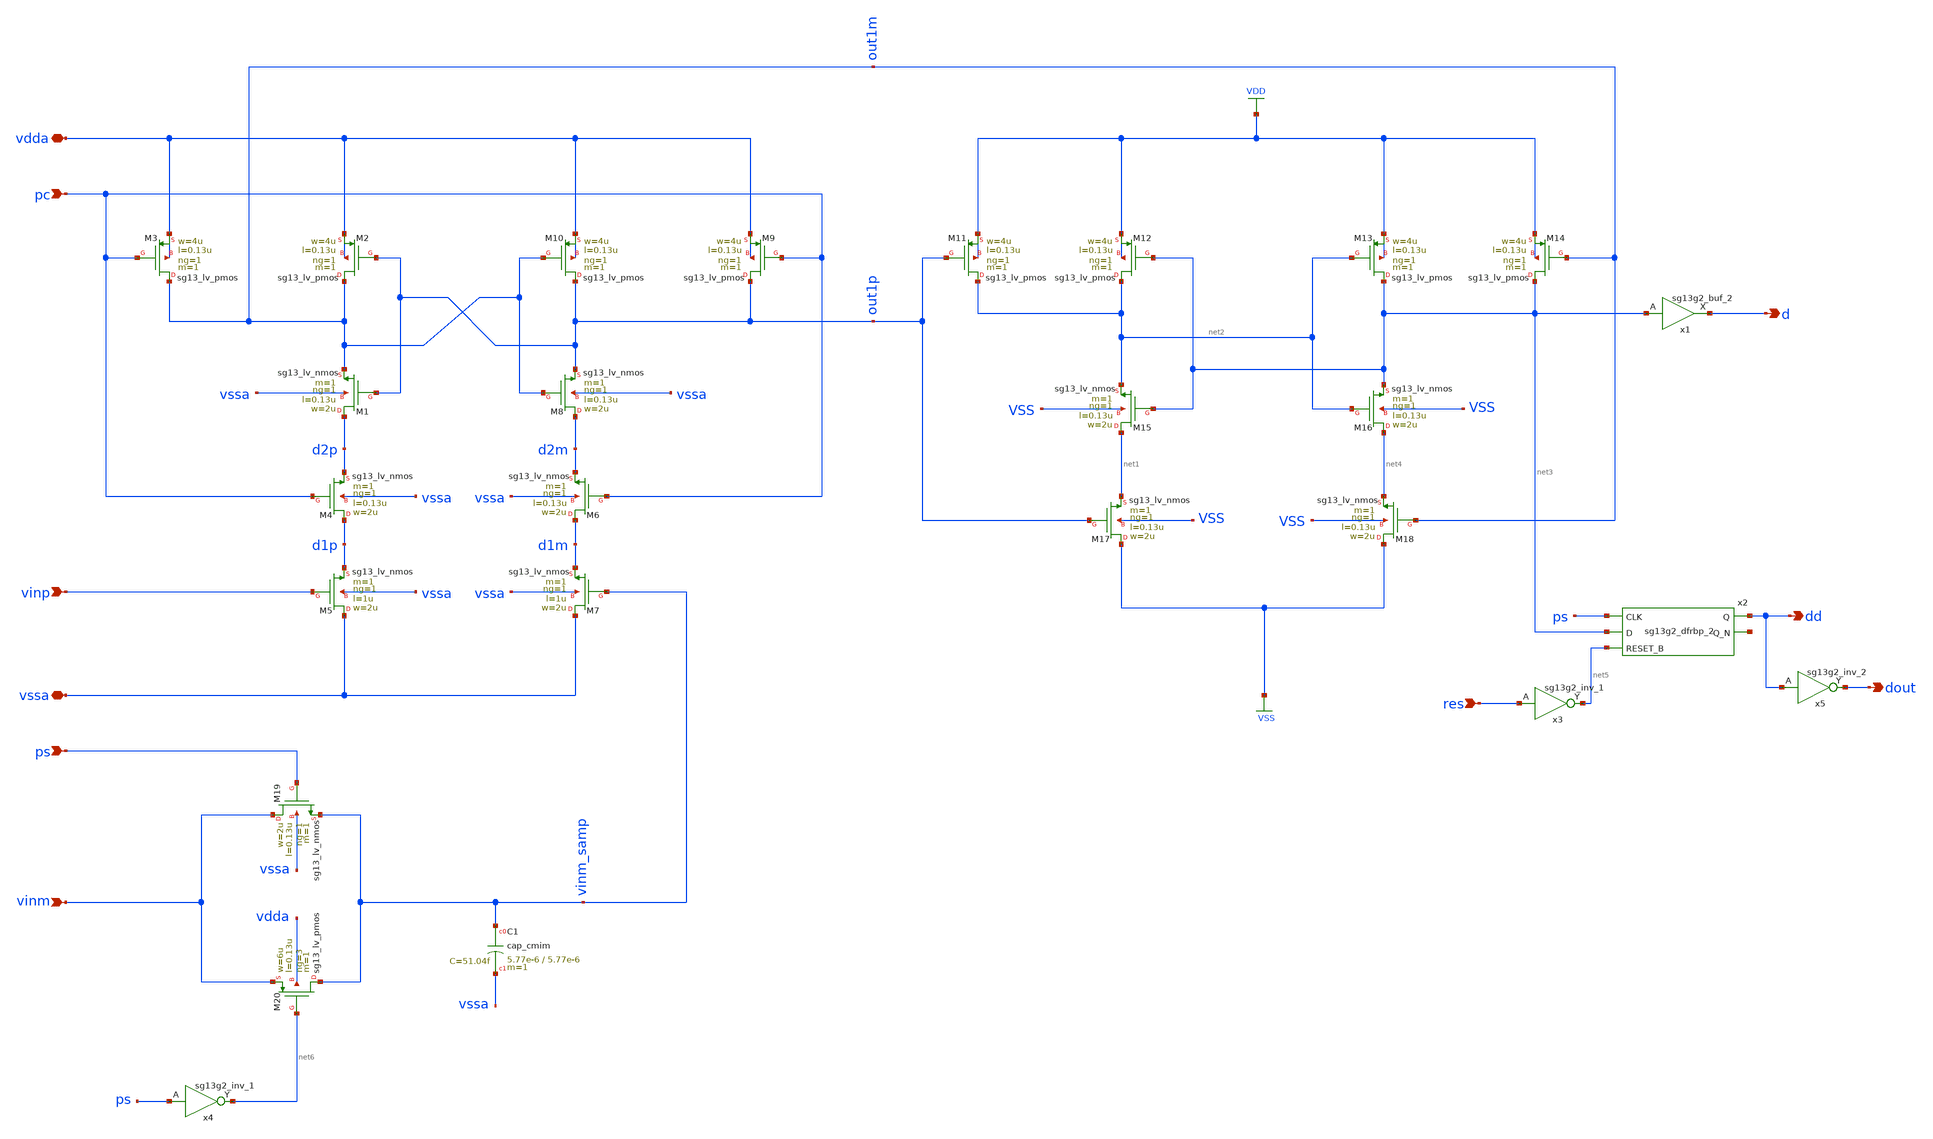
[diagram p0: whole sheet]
** sch_path: 5_Design/4_Layout/Team 3/xschem/comp_Team3.sch
* IHP-GmbH/IHP-Open-PDK/ihp-sg13g2/libs.tech/xschem/sg13g2_stdcells/sg13g2_inv_2.sch:
* Copyright 2023 IHP PDK Authors
* Licensed under the Apache License, Version 2.0 (the "License");
**.subckt comp_Team3 pc vssa vdda vinp vinm d res dd ps dout
*.ipin pc
*.iopin vssa
*.iopin vdda
*.ipin vinp
*.ipin vinm
*.opin d
*.ipin res
*.opin dd
*.ipin ps
*.opin dout
XM1 d2p out1p out1m vssa sg13_lv_nmos w=2u l=0.13u ng=1 m=1 mm_ok=1
XM2 out1m out1p vdda vdda sg13_lv_pmos w=4u l=0.13u ng=1 m=1 mm_ok=1
XM3 out1m pc vdda vdda sg13_lv_pmos w=4u l=0.13u ng=1 m=1 mm_ok=1
XM4 d1p pc d2p vssa sg13_lv_nmos w=2u l=0.13u ng=1 m=1 mm_ok=1
XM5 vssa vinp d1p vssa sg13_lv_nmos w=2u l=1u ng=1 m=1 mm_ok=1
XM6 d1m pc d2m vssa sg13_lv_nmos w=2u l=0.13u ng=1 m=1 mm_ok=1
XM7 vssa vinm_samp d1m vssa sg13_lv_nmos w=2u l=1u ng=1 m=1 mm_ok=1
XM8 d2m out1m out1p vssa sg13_lv_nmos w=2u l=0.13u ng=1 m=1 mm_ok=1
XM9 out1p pc vdda vdda sg13_lv_pmos w=4u l=0.13u ng=1 m=1 mm_ok=1
XM10 out1p out1m vdda vdda sg13_lv_pmos w=4u l=0.13u ng=1 m=1 mm_ok=1
XM11 net2 out1p VDD VDD sg13_lv_pmos w=4u l=0.13u ng=1 m=1 mm_ok=1
XM12 net2 net3 VDD VDD sg13_lv_pmos w=4u l=0.13u ng=1 m=1 mm_ok=1
XM13 net3 net2 VDD VDD sg13_lv_pmos w=4u l=0.13u ng=1 m=1 mm_ok=1
XM14 net3 out1m VDD VDD sg13_lv_pmos w=4u l=0.13u ng=1 m=1 mm_ok=1
XM15 net1 net3 net2 VSS sg13_lv_nmos w=2u l=0.13u ng=1 m=1 mm_ok=1
XM16 net4 net2 net3 VSS sg13_lv_nmos w=2u l=0.13u ng=1 m=1 mm_ok=1
XM17 VSS out1p net1 VSS sg13_lv_nmos w=2u l=0.13u ng=1 m=1 mm_ok=1
XM18 VSS out1m net4 VSS sg13_lv_nmos w=2u l=0.13u ng=1 m=1 mm_ok=1
x1 d net3 VDD VSS sg13g2_buf_2
x2 dd net7 ps net3 net5 VDD VSS sg13g2_dfrbp_2
x3 net5 res VDD VSS sg13g2_inv_1
XM19 vinm ps vinm_samp vssa sg13_lv_nmos w=2u l=0.13u ng=1 m=1 mm_ok=1
XM20 vinm_samp net6 vinm vdda sg13_lv_pmos w=6u l=0.13u ng=3 m=1 mm_ok=1
x4 net6 ps VDD VSS sg13g2_inv_1
x5 dout dd VDD VSS sg13g2_inv_2
XC1 vinm_samp vssa cap_cmim w=5.77e-6 l=5.77e-6 m=1 mm_ok=1
**.ends

* expanding   symbol:  sg13g2_stdcells/sg13g2_buf_2.sym # of pins=2
** sym_path: sg13g2_stdcells/sg13g2_buf_2.sym
** sch_path: sg13g2_stdcells/sg13g2_buf_2.sch
.subckt sg13g2_buf_2 X A VDD VSS
*.ipin A
*.opin X
*.iopin VDD
*.iopin VSS
XM1 net1 A VSS VSS sg13_lv_nmos w=640.00n l=130.00n ng=1 m=1 mm_ok=1
XM2 X net1 VSS VSS sg13_lv_nmos w=1.48u l=130.00n ng=2 m=1 mm_ok=1
XM3 net1 A VDD VDD sg13_lv_pmos w=1.000u l=130.00n ng=1 m=1 mm_ok=1
XM4 X net1 VDD VDD sg13_lv_pmos w=2.24u l=130.00n ng=2 m=1 mm_ok=1
.ends


* expanding   symbol:  sg13g2_stdcells/sg13g2_dfrbp_2.sym # of pins=5
** sym_path: sg13g2_stdcells/sg13g2_dfrbp_2.sym
** sch_path: sg13g2_stdcells/sg13g2_dfrbp_2.sch
.subckt sg13g2_dfrbp_2 Q Q_N CLK D RESET_B VDD VSS
*.ipin D
*.ipin RESET_B
*.ipin CLK
*.opin Q
*.opin Q_N
*.iopin VDD
*.iopin VSS
XM1 Db D net12 VSS sg13_lv_nmos w=420.00n l=130.00n ng=1 m=1 mm_ok=1
XM2 net12 RESET_B VSS VSS sg13_lv_nmos w=420.00n l=130.00n ng=1 m=1 mm_ok=1
XM3 net2 clkneg net11 VSS sg13_lv_nmos w=420.00n l=130.00n ng=1 m=1 mm_ok=1
XM4 net11 net3 VSS VSS sg13_lv_nmos w=420.00n l=130.00n ng=1 m=1 mm_ok=1
XM5 net3 net2 net7 VSS sg13_lv_nmos w=420.00n l=130.00n ng=1 m=1 mm_ok=1
XM6 net7 RESET_B VSS VSS sg13_lv_nmos w=420.00n l=130.00n ng=1 m=1 mm_ok=1
XM7 Q_N net2 VSS VSS sg13_lv_nmos w=1.48u l=130.00n ng=2 m=1 mm_ok=1
XM8 net1 net2 VSS VSS sg13_lv_nmos w=640.00n l=130.00n ng=1 m=1 mm_ok=1
XM9 Q net1 VSS VSS sg13_lv_nmos w=1.48u l=130.00n ng=2 m=1 mm_ok=1
XM10 clkneg CLK VSS VSS sg13_lv_nmos w=740.00n l=130.00n ng=1 m=1 mm_ok=1
XM11 clkpos clkneg VSS VSS sg13_lv_nmos w=740.00n l=130.00n ng=1 m=1 mm_ok=1
XM12 Db clkneg net4 VSS sg13_lv_nmos w=420.00n l=130.00n ng=1 m=1 mm_ok=1
XM13 net4 clkpos net10 VSS sg13_lv_nmos w=420.00n l=130.00n ng=1 m=1 mm_ok=1
XM14 net10 net5 net6 VSS sg13_lv_nmos w=420.00n l=130.00n ng=1 m=1 mm_ok=1
XM15 net6 RESET_B VSS VSS sg13_lv_nmos w=420.00n l=130.00n ng=1 m=1 mm_ok=1
XM16 net5 net4 VSS VSS sg13_lv_nmos w=740.00n l=130.00n ng=1 m=1 mm_ok=1
XM17 net5 clkpos net2 VSS sg13_lv_nmos w=740.00n l=130.00n ng=1 m=1 mm_ok=1
XM18 Db RESET_B VDD VDD sg13_lv_pmos w=420.00n l=130.00n ng=1 m=1 mm_ok=1
XM19 Db D VDD VDD sg13_lv_pmos w=420.00n l=130.00n ng=1 m=1 mm_ok=1
XM20 net9 net3 VDD VDD sg13_lv_pmos w=420.00n l=130.00n ng=1 m=1 mm_ok=1
XM21 net2 clkpos net9 VDD sg13_lv_pmos w=420.00n l=130.00n ng=1 m=1 mm_ok=1
XM22 net3 net2 VDD VDD sg13_lv_pmos w=420.00n l=130.00n ng=1 m=1 mm_ok=1
XM23 net3 RESET_B VDD VDD sg13_lv_pmos w=420.00n l=130.00n ng=1 m=1 mm_ok=1
XM24 Q_N net2 VDD VDD sg13_lv_pmos w=2.24u l=130.00n ng=2 m=1 mm_ok=1
XM25 net1 net2 VDD VDD sg13_lv_pmos w=1.000u l=130.00n ng=1 m=1 mm_ok=1
XM26 Q net1 VDD VDD sg13_lv_pmos w=2.24u l=130.00n ng=2 m=1 mm_ok=1
XM27 clkneg CLK VDD VDD sg13_lv_pmos w=1.12u l=130.00n ng=1 m=1 mm_ok=1
XM28 clkpos clkneg VDD VDD sg13_lv_pmos w=1.12u l=130.00n ng=1 m=1 mm_ok=1
XM29 Db clkpos net4 VDD sg13_lv_pmos w=420.00n l=130.00n ng=1 m=1 mm_ok=1
XM30 net8 net5 VDD VDD sg13_lv_pmos w=420.00n l=130.00n ng=1 m=1 mm_ok=1
XM31 net4 clkneg net8 VDD sg13_lv_pmos w=420.00n l=130.00n ng=1 m=1 mm_ok=1
XM32 net4 RESET_B VDD VDD sg13_lv_pmos w=420.00n l=130.00n ng=1 m=1 mm_ok=1
XM33 net5 net4 VDD VDD sg13_lv_pmos w=1.000u l=130.00n ng=1 m=1 mm_ok=1
XM34 net5 clkneg net2 VDD sg13_lv_pmos w=1.000u l=130.00n ng=1 m=1 mm_ok=1
.ends


* expanding   symbol:  sg13g2_stdcells/sg13g2_inv_1.sym # of pins=2
** sym_path: sg13g2_stdcells/sg13g2_inv_1.sym
** sch_path: sg13g2_stdcells/sg13g2_inv_1.sch
.subckt sg13g2_inv_1 Y A VDD VSS
*.opin Y
*.ipin A
*.iopin VDD
*.iopin VSS
XM1 Y A VSS VSS sg13_lv_nmos w=740.00n l=130.00n ng=1 m=1 mm_ok=1
XM2 Y A VDD VDD sg13_lv_pmos w=1.12u l=130.00n ng=1 m=1 mm_ok=1
.ends


* expanding   symbol:  sg13g2_stdcells/sg13g2_inv_2.sym # of pins=2
** sym_path: sg13g2_stdcells/sg13g2_inv_2.sym
** sch_path: sg13g2_stdcells/sg13g2_inv_2.sch
.subckt sg13g2_inv_2 Y A VDD VSS
*.opin Y
*.ipin A
*.iopin VDD
*.iopin VSS
XM1 Y A VSS VSS sg13_lv_nmos w=1.48u l=130.00n ng=2 m=1 mm_ok=1
XM2 Y A VDD VDD sg13_lv_pmos w=2.24u l=130.00n ng=2 m=1 mm_ok=1
.ends

.GLOBAL VDD
.GLOBAL VSS
.end
